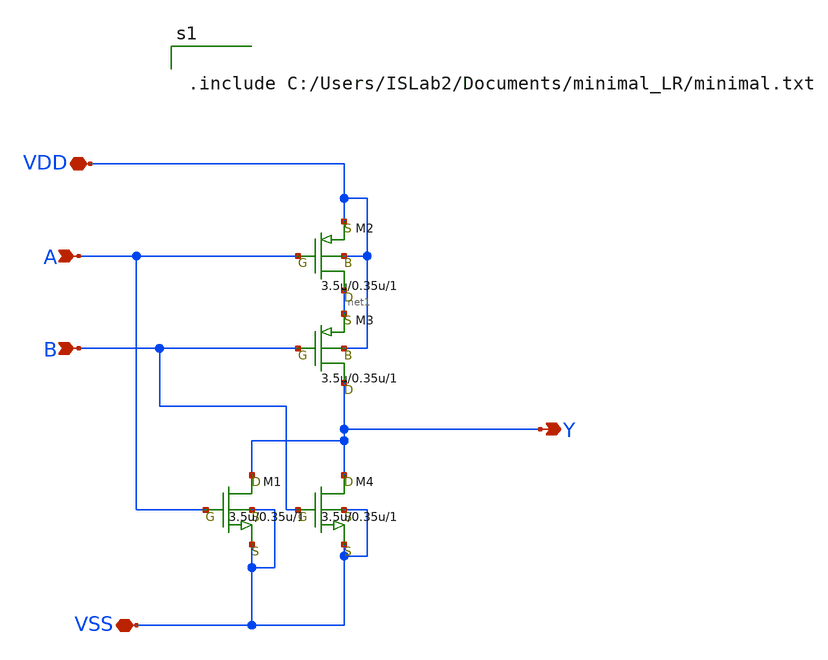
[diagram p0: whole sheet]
** sch_path: NOR.sch
**.subckt NOR VDD A B VSS Y
*.iopin VDD
*.ipin A
*.ipin B
*.iopin VSS
*.opin Y
M1 Y A VSS VSS nch w=3.5u l=0.35u as=0 ps=0 ad=0 pd=0 m=1
M2 net1 A VDD VDD pch w=3.5u l=0.35u as=0 ps=0 ad=0 pd=0 m=1
M3 Y B net1 VDD pch w=3.5u l=0.35u as=0 ps=0 ad=0 pd=0 m=1
M4 Y B VSS VSS nch w=3.5u l=0.35u as=0 ps=0 ad=0 pd=0 m=1
**** begin user architecture code


.include C:/Users/ISLab2/Documents/minimal_LR/minimal.txt

**** end user architecture code
**.ends
.end
